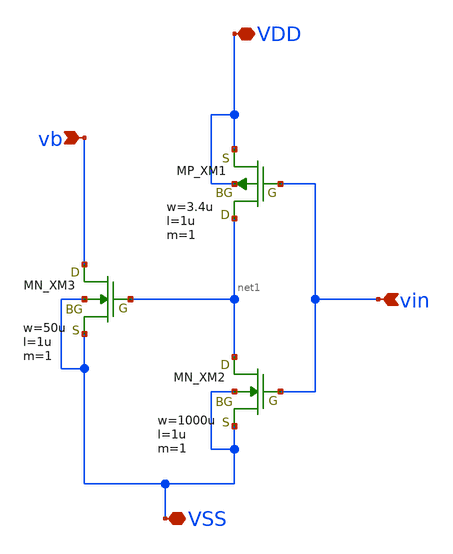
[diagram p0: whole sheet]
** sch_path: schematic/20250924_OSS_Workshop/ishikai/CS/cs_startup.sch
**.subckt cs_startup VDD VSS vin vb
*.iopin VDD
*.iopin VSS
*.ipin vin
*.ipin vb
XM1 net1 vin VDD VDD PMOS w=3.4u l=1u as=0 ad=0 ps=0 pd=0 nrd=0 nrs=0 m=1
XM2 net1 vin VSS VSS NMOS w=1000u l=1u as=0 ad=0 ps=0 pd=0 nrd=0 nrs=0 m=1
XM3 vb net1 VSS VSS NMOS w=50u l=1u as=0 ad=0 ps=0 pd=0 nrd=0 nrs=0 m=1
**.ends
.end
